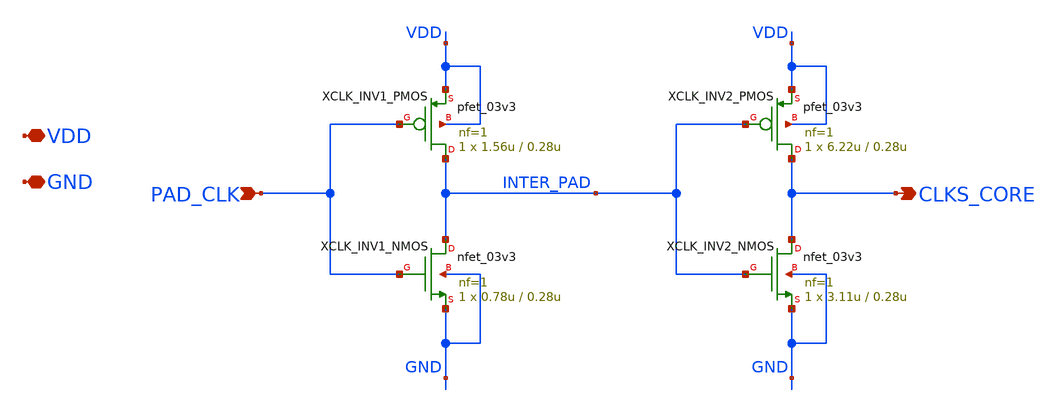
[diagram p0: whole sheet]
** sch_path: verification/a44_w5p29_trans_driver/01_CURRENT_CIRCUIT_FILES/xschem/A44_CLKS_BUFFER.sch
**.subckt A44_CLKS_BUFFER PAD_CLK CLKS_CORE VDD GND
*.ipin PAD_CLK
*.opin CLKS_CORE
*.iopin VDD
*.iopin GND
XCLK_INV1_NMOS INTER_PAD PAD_CLK GND GND nfet_03v3 L=0.28u W=0.78u nf=1 ad='int((nf+1)/2) * W/nf * 0.18u'
+ as='int((nf+2)/2) * W/nf * 0.18u' pd='2*int((nf+1)/2) * (W/nf + 0.18u)' ps='2*int((nf+2)/2) * (W/nf + 0.18u)'
+ nrd='0.18u / W' nrs='0.18u / W' sa=0 sb=0 sd=0 m=1
XCLK_INV1_PMOS INTER_PAD PAD_CLK VDD VDD pfet_03v3 L=0.28u W=1.56u nf=1 ad='int((nf+1)/2) * W/nf * 0.18u'
+ as='int((nf+2)/2) * W/nf * 0.18u' pd='2*int((nf+1)/2) * (W/nf + 0.18u)' ps='2*int((nf+2)/2) * (W/nf + 0.18u)'
+ nrd='0.18u / W' nrs='0.18u / W' sa=0 sb=0 sd=0 m=1
XCLK_INV2_NMOS CLKS_CORE INTER_PAD GND GND nfet_03v3 L=0.28u W=3.11u nf=1 ad='int((nf+1)/2) * W/nf * 0.18u'
+ as='int((nf+2)/2) * W/nf * 0.18u' pd='2*int((nf+1)/2) * (W/nf + 0.18u)' ps='2*int((nf+2)/2) * (W/nf + 0.18u)'
+ nrd='0.18u / W' nrs='0.18u / W' sa=0 sb=0 sd=0 m=1
XCLK_INV2_PMOS CLKS_CORE INTER_PAD VDD VDD pfet_03v3 L=0.28u W=6.22u nf=1 ad='int((nf+1)/2) * W/nf * 0.18u'
+ as='int((nf+2)/2) * W/nf * 0.18u' pd='2*int((nf+1)/2) * (W/nf + 0.18u)' ps='2*int((nf+2)/2) * (W/nf + 0.18u)'
+ nrd='0.18u / W' nrs='0.18u / W' sa=0 sb=0 sd=0 m=1
**.ends
.end
